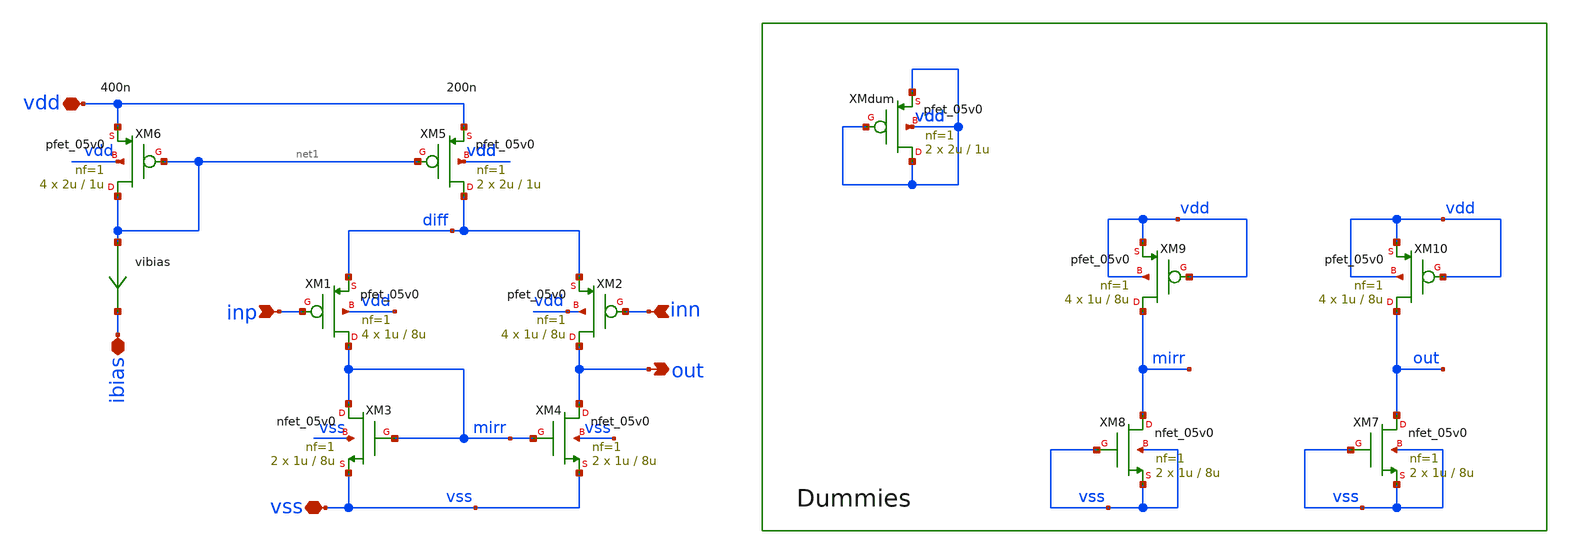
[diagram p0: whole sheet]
** sch_path: xschem/bandgap_amp.sch
**.subckt bandgap_amp out inp inn vdd vss ibias
*.opin out
*.ipin inp
*.ipin inn
*.iopin vdd
*.iopin vss
*.iopin ibias
vibias net1 ibias 0
.save i(vibias)
XM4 out mirr vss vss nfet_05v0 L=8u W=1u nf=1 ad='int((nf+1)/2) * W/nf * 0.18u' as='int((nf+2)/2) * W/nf * 0.18u'
+ pd='2*int((nf+1)/2) * (W/nf + 0.18u)' ps='2*int((nf+2)/2) * (W/nf + 0.18u)' nrd='0.18u / W' nrs='0.18u / W'
+ sa=0 sb=0 sd=0 m=2
XM3 mirr mirr vss vss nfet_05v0 L=8u W=1u nf=1 ad='int((nf+1)/2) * W/nf * 0.18u' as='int((nf+2)/2) * W/nf * 0.18u'
+ pd='2*int((nf+1)/2) * (W/nf + 0.18u)' ps='2*int((nf+2)/2) * (W/nf + 0.18u)' nrd='0.18u / W' nrs='0.18u / W'
+ sa=0 sb=0 sd=0 m=2
XM1 mirr inp diff vdd pfet_05v0 L=8u W=1u nf=1 ad='int((nf+1)/2) * W/nf * 0.18u' as='int((nf+2)/2) * W/nf * 0.18u'
+ pd='2*int((nf+1)/2) * (W/nf + 0.18u)' ps='2*int((nf+2)/2) * (W/nf + 0.18u)' nrd='0.18u / W' nrs='0.18u / W'
+ sa=0 sb=0 sd=0 m=4 par=4
XM2 out inn diff vdd pfet_05v0 L=8u W=1u nf=1 ad='int((nf+1)/2) * W/nf * 0.18u' as='int((nf+2)/2) * W/nf * 0.18u'
+ pd='2*int((nf+1)/2) * (W/nf + 0.18u)' ps='2*int((nf+2)/2) * (W/nf + 0.18u)' nrd='0.18u / W' nrs='0.18u / W'
+ sa=0 sb=0 sd=0 m=4 par=4
XM5 diff net1 vdd vdd pfet_05v0 L=1u W=2u nf=1 ad='int((nf+1)/2) * W/nf * 0.18u' as='int((nf+2)/2) * W/nf * 0.18u'
+ pd='2*int((nf+1)/2) * (W/nf + 0.18u)' ps='2*int((nf+2)/2) * (W/nf + 0.18u)' nrd='0.18u / W' nrs='0.18u / W'
+ sa=0 sb=0 sd=0 m=2 par=2
XM6 net1 net1 vdd vdd pfet_05v0 L=1u W=2u nf=1 ad='int((nf+1)/2) * W/nf * 0.18u' as='int((nf+2)/2) * W/nf * 0.18u'
+ pd='2*int((nf+1)/2) * (W/nf + 0.18u)' ps='2*int((nf+2)/2) * (W/nf + 0.18u)' nrd='0.18u / W' nrs='0.18u / W'
+ sa=0 sb=0 sd=0 m=4 par=4
XMdum vdd vdd vdd vdd pfet_05v0 L=1u W=2u nf=1 ad='int((nf+1)/2) * W/nf * 0.18u' as='int((nf+2)/2) * W/nf * 0.18u'
+ pd='2*int((nf+1)/2) * (W/nf + 0.18u)' ps='2*int((nf+2)/2) * (W/nf + 0.18u)' nrd='0.18u / W' nrs='0.18u / W'
+ sa=0 sb=0 sd=0 m=2 par=2
XM7 out vss vss vss nfet_05v0 L=8u W=1u nf=1 ad='int((nf+1)/2) * W/nf * 0.18u' as='int((nf+2)/2) * W/nf * 0.18u'
+ pd='2*int((nf+1)/2) * (W/nf + 0.18u)' ps='2*int((nf+2)/2) * (W/nf + 0.18u)' nrd='0.18u / W' nrs='0.18u / W'
+ sa=0 sb=0 sd=0 m=2
XM8 mirr vss vss vss nfet_05v0 L=8u W=1u nf=1 ad='int((nf+1)/2) * W/nf * 0.18u' as='int((nf+2)/2) * W/nf * 0.18u'
+ pd='2*int((nf+1)/2) * (W/nf + 0.18u)' ps='2*int((nf+2)/2) * (W/nf + 0.18u)' nrd='0.18u / W' nrs='0.18u / W'
+ sa=0 sb=0 sd=0 m=2
XM9 mirr vdd vdd vdd pfet_05v0 L=8u W=1u nf=1 ad='int((nf+1)/2) * W/nf * 0.18u' as='int((nf+2)/2) * W/nf * 0.18u'
+ pd='2*int((nf+1)/2) * (W/nf + 0.18u)' ps='2*int((nf+2)/2) * (W/nf + 0.18u)' nrd='0.18u / W' nrs='0.18u / W'
+ sa=0 sb=0 sd=0 m=4 par=4
XM10 out vdd vdd vdd pfet_05v0 L=8u W=1u nf=1 ad='int((nf+1)/2) * W/nf * 0.18u' as='int((nf+2)/2) * W/nf * 0.18u'
+ pd='2*int((nf+1)/2) * (W/nf + 0.18u)' ps='2*int((nf+2)/2) * (W/nf + 0.18u)' nrd='0.18u / W' nrs='0.18u / W'
+ sa=0 sb=0 sd=0 m=4 par=4
**.ends
.end
